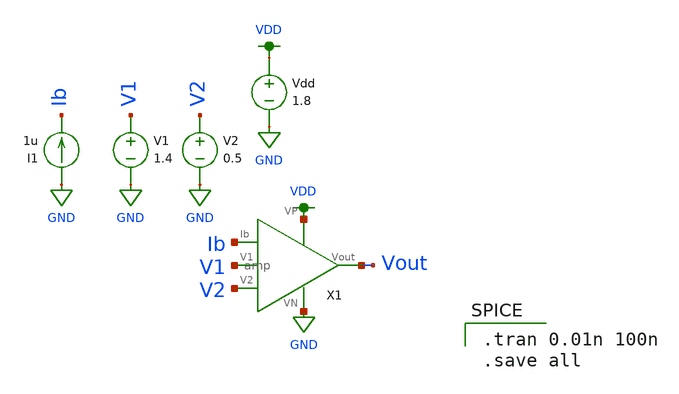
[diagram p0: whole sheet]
** sch_path: mp3/schematic/amp_tran.sch
**.subckt amp_tran
X1 Ib V1 V2 VDD GND Vout amp
V1 V1 GND 1.4
V2 V2 GND 0.5
I1 GND Ib 1u
Vdd VDD GND 1.8
**** begin user architecture code

.option wnflag=1
.lib ~/skywater/skywater-pdk/libraries/sky130_fd_pr_ngspice/latest/models/sky130.lib.spice tt


.tran 0.01n 100n
.save all

**** end user architecture code
**.ends
.GLOBAL GND
.GLOBAL VDD
.end
